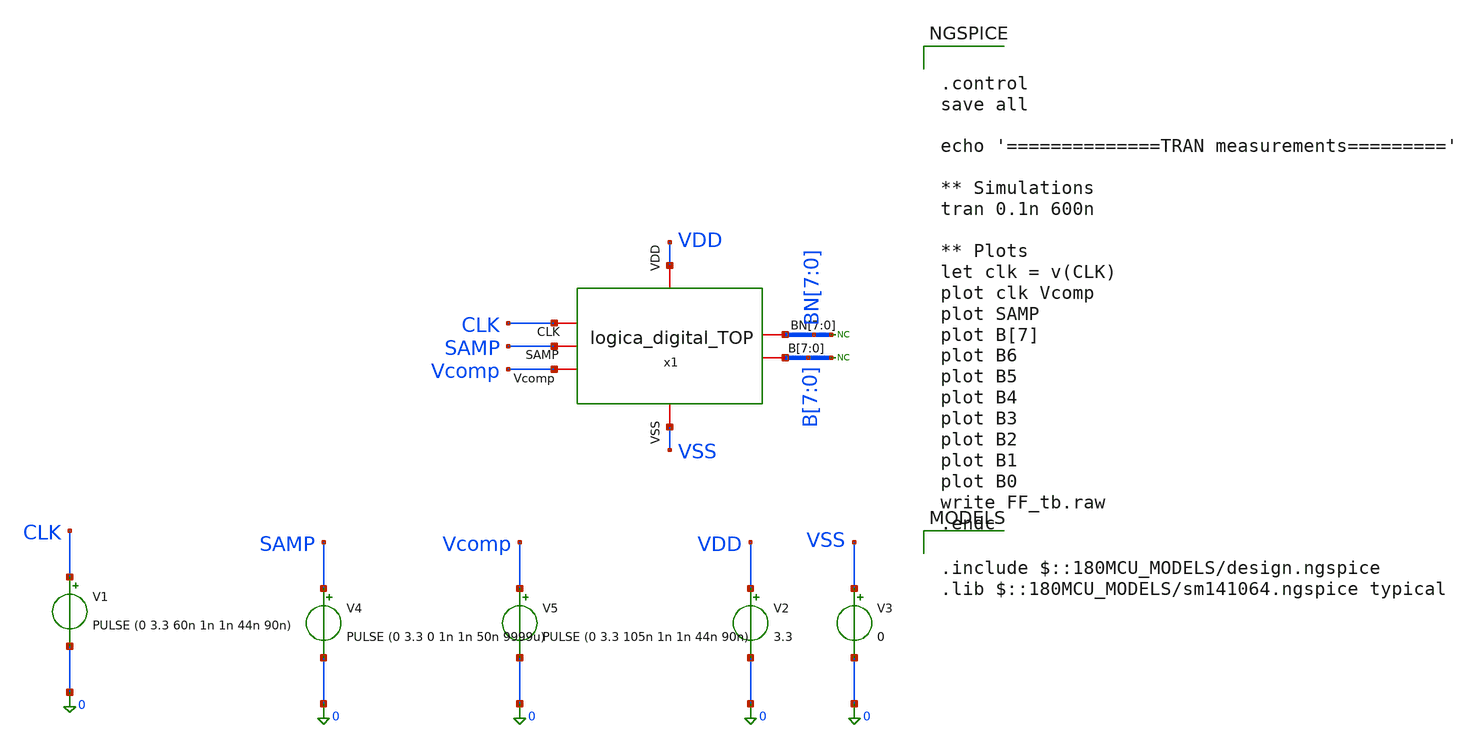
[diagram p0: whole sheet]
** sch_path: designs/sar_adc/digital/logica_digital_TOP/xschem/logica_digital_TOP_tb.sch
**.subckt logica_digital_TOP_tb
x1 VDD VSS CLK SAMP Vcomp BN[7] BN[6] BN[5] BN[4] BN[3] BN[2] BN[1] BN[0] B[7] B[6] B[5] B[4] B[3]
+ B[2] B[1] B[0] logica_digital_TOP
V1 CLK 0 PULSE (0 3.3 60n 1n 1n 44n 90n)
V2 VDD 0 3.3
V3 VSS 0 0
V5 Vcomp 0 PULSE (0 3.3 105n 1n 1n 44n 90n)
V4 SAMP 0 PULSE (0 3.3 0 1n 1n 50n 9999u)
* noconn B[7:0]
* noconn BN[7:0]
**** begin user architecture code


.control
save all

echo '==============TRAN measurements========='

** Simulations
tran 0.1n 600n

** Plots
let clk = v(CLK)
plot clk Vcomp
plot SAMP
plot B[7]
plot B6
plot B5
plot B4
plot B3
plot B2
plot B1
plot B0
write FF_tb.raw
.endc



.include $::180MCU_MODELS/design.ngspice
.lib $::180MCU_MODELS/sm141064.ngspice typical

**** end user architecture code
**.ends
.end
